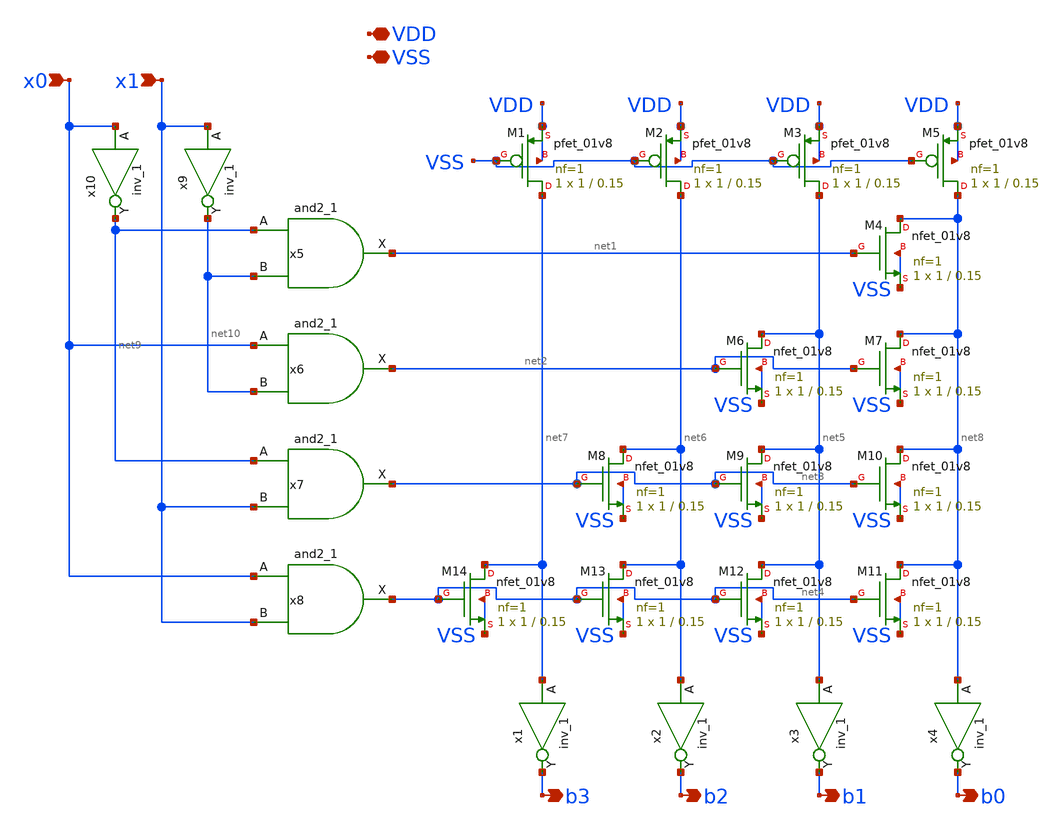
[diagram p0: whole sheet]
** sch_path: xschem/NOR_ROM_2bit.sch
**.subckt NOR_ROM_2bit VDD VSS x0 b3 x1 b2 b1 b0
*.iopin VDD
*.iopin VSS
*.ipin x0
*.opin b3
*.ipin x1
*.opin b2
*.opin b1
*.opin b0
XM4 net8 net1 VSS VSS sky130_fd_pr__nfet_01v8 L=0.15 W=1 nf=1 ad='int((nf+1)/2) * W/nf * 0.29' as='int((nf+2)/2) * W/nf * 0.29'
+ pd='2*int((nf+1)/2) * (W/nf + 0.29)' ps='2*int((nf+2)/2) * (W/nf + 0.29)' nrd='0.29 / W' nrs='0.29 / W'
+ sa=0 sb=0 sd=0 mult=1 m=1
XM6 net5 net2 VSS VSS sky130_fd_pr__nfet_01v8 L=0.15 W=1 nf=1 ad='int((nf+1)/2) * W/nf * 0.29' as='int((nf+2)/2) * W/nf * 0.29'
+ pd='2*int((nf+1)/2) * (W/nf + 0.29)' ps='2*int((nf+2)/2) * (W/nf + 0.29)' nrd='0.29 / W' nrs='0.29 / W'
+ sa=0 sb=0 sd=0 mult=1 m=1
XM7 net8 net2 VSS VSS sky130_fd_pr__nfet_01v8 L=0.15 W=1 nf=1 ad='int((nf+1)/2) * W/nf * 0.29' as='int((nf+2)/2) * W/nf * 0.29'
+ pd='2*int((nf+1)/2) * (W/nf + 0.29)' ps='2*int((nf+2)/2) * (W/nf + 0.29)' nrd='0.29 / W' nrs='0.29 / W'
+ sa=0 sb=0 sd=0 mult=1 m=1
XM8 net6 net3 VSS VSS sky130_fd_pr__nfet_01v8 L=0.15 W=1 nf=1 ad='int((nf+1)/2) * W/nf * 0.29' as='int((nf+2)/2) * W/nf * 0.29'
+ pd='2*int((nf+1)/2) * (W/nf + 0.29)' ps='2*int((nf+2)/2) * (W/nf + 0.29)' nrd='0.29 / W' nrs='0.29 / W'
+ sa=0 sb=0 sd=0 mult=1 m=1
XM9 net5 net3 VSS VSS sky130_fd_pr__nfet_01v8 L=0.15 W=1 nf=1 ad='int((nf+1)/2) * W/nf * 0.29' as='int((nf+2)/2) * W/nf * 0.29'
+ pd='2*int((nf+1)/2) * (W/nf + 0.29)' ps='2*int((nf+2)/2) * (W/nf + 0.29)' nrd='0.29 / W' nrs='0.29 / W'
+ sa=0 sb=0 sd=0 mult=1 m=1
XM10 net8 net3 VSS VSS sky130_fd_pr__nfet_01v8 L=0.15 W=1 nf=1 ad='int((nf+1)/2) * W/nf * 0.29' as='int((nf+2)/2) * W/nf * 0.29'
+ pd='2*int((nf+1)/2) * (W/nf + 0.29)' ps='2*int((nf+2)/2) * (W/nf + 0.29)' nrd='0.29 / W' nrs='0.29 / W'
+ sa=0 sb=0 sd=0 mult=1 m=1
XM11 net8 net4 VSS VSS sky130_fd_pr__nfet_01v8 L=0.15 W=1 nf=1 ad='int((nf+1)/2) * W/nf * 0.29' as='int((nf+2)/2) * W/nf * 0.29'
+ pd='2*int((nf+1)/2) * (W/nf + 0.29)' ps='2*int((nf+2)/2) * (W/nf + 0.29)' nrd='0.29 / W' nrs='0.29 / W'
+ sa=0 sb=0 sd=0 mult=1 m=1
XM12 net5 net4 VSS VSS sky130_fd_pr__nfet_01v8 L=0.15 W=1 nf=1 ad='int((nf+1)/2) * W/nf * 0.29' as='int((nf+2)/2) * W/nf * 0.29'
+ pd='2*int((nf+1)/2) * (W/nf + 0.29)' ps='2*int((nf+2)/2) * (W/nf + 0.29)' nrd='0.29 / W' nrs='0.29 / W'
+ sa=0 sb=0 sd=0 mult=1 m=1
XM13 net6 net4 VSS VSS sky130_fd_pr__nfet_01v8 L=0.15 W=1 nf=1 ad='int((nf+1)/2) * W/nf * 0.29' as='int((nf+2)/2) * W/nf * 0.29'
+ pd='2*int((nf+1)/2) * (W/nf + 0.29)' ps='2*int((nf+2)/2) * (W/nf + 0.29)' nrd='0.29 / W' nrs='0.29 / W'
+ sa=0 sb=0 sd=0 mult=1 m=1
XM14 net7 net4 VSS VSS sky130_fd_pr__nfet_01v8 L=0.15 W=1 nf=1 ad='int((nf+1)/2) * W/nf * 0.29' as='int((nf+2)/2) * W/nf * 0.29'
+ pd='2*int((nf+1)/2) * (W/nf + 0.29)' ps='2*int((nf+2)/2) * (W/nf + 0.29)' nrd='0.29 / W' nrs='0.29 / W'
+ sa=0 sb=0 sd=0 mult=1 m=1
x1 net7 VGND VNB VPB VPWR b3 sky130_fd_sc_hd__inv_1
x2 net6 VGND VNB VPB VPWR b2 sky130_fd_sc_hd__inv_1
x3 net5 VGND VNB VPB VPWR b1 sky130_fd_sc_hd__inv_1
x4 net8 VGND VNB VPB VPWR b0 sky130_fd_sc_hd__inv_1
x5 net9 net10 VGND VNB VPB VPWR net1 sky130_fd_sc_hd__and2_1
x6 x0 net10 VGND VNB VPB VPWR net2 sky130_fd_sc_hd__and2_1
x7 net9 x1 VGND VNB VPB VPWR net3 sky130_fd_sc_hd__and2_1
x8 x0 x1 VGND VNB VPB VPWR net4 sky130_fd_sc_hd__and2_1
x9 x1 VGND VNB VPB VPWR net10 sky130_fd_sc_hd__inv_1
x10 x0 VGND VNB VPB VPWR net9 sky130_fd_sc_hd__inv_1
XM1 net7 VSS VDD VDD sky130_fd_pr__pfet_01v8 L=0.15 W=1 nf=1 ad='int((nf+1)/2) * W/nf * 0.29' as='int((nf+2)/2) * W/nf * 0.29'
+ pd='2*int((nf+1)/2) * (W/nf + 0.29)' ps='2*int((nf+2)/2) * (W/nf + 0.29)' nrd='0.29 / W' nrs='0.29 / W'
+ sa=0 sb=0 sd=0 mult=1 m=1
XM2 net6 VSS VDD VDD sky130_fd_pr__pfet_01v8 L=0.15 W=1 nf=1 ad='int((nf+1)/2) * W/nf * 0.29' as='int((nf+2)/2) * W/nf * 0.29'
+ pd='2*int((nf+1)/2) * (W/nf + 0.29)' ps='2*int((nf+2)/2) * (W/nf + 0.29)' nrd='0.29 / W' nrs='0.29 / W'
+ sa=0 sb=0 sd=0 mult=1 m=1
XM3 net5 VSS VDD VDD sky130_fd_pr__pfet_01v8 L=0.15 W=1 nf=1 ad='int((nf+1)/2) * W/nf * 0.29' as='int((nf+2)/2) * W/nf * 0.29'
+ pd='2*int((nf+1)/2) * (W/nf + 0.29)' ps='2*int((nf+2)/2) * (W/nf + 0.29)' nrd='0.29 / W' nrs='0.29 / W'
+ sa=0 sb=0 sd=0 mult=1 m=1
XM5 net8 VSS VDD VDD sky130_fd_pr__pfet_01v8 L=0.15 W=1 nf=1 ad='int((nf+1)/2) * W/nf * 0.29' as='int((nf+2)/2) * W/nf * 0.29'
+ pd='2*int((nf+1)/2) * (W/nf + 0.29)' ps='2*int((nf+2)/2) * (W/nf + 0.29)' nrd='0.29 / W' nrs='0.29 / W'
+ sa=0 sb=0 sd=0 mult=1 m=1
**.ends
.end
